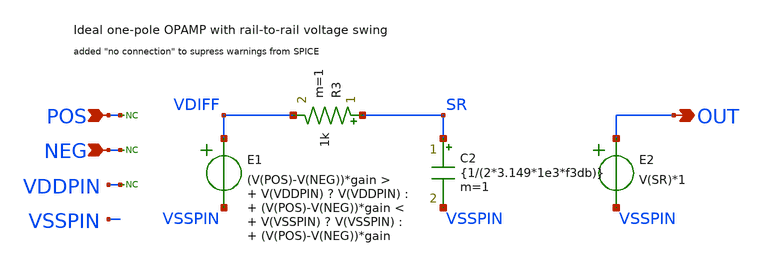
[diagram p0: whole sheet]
** sch_path: opamp_onepole.sch
**.subckt opamp_onepole OUT POS NEG
*.opin OUT
*.ipin POS
*.ipin NEG
E1 VDIFF VSSPIN VOL=' (V(POS)-V(NEG))*gain > V(VDDPIN) ? V(VDDPIN) : (V(POS)-V(NEG))*gain < V(VSSPIN) ? V(VSSPIN) : (V(POS)-V(NEG))*gain '
R3 SR VDIFF 1k m=1
C2 SR VSSPIN {1/(2*3.149*1e3*f3db)} m=1
E2 OUT VSSPIN VOL=' V(SR)*1 '
* noconn POS
* noconn NEG
* noconn VDDPIN
**.ends
.end
